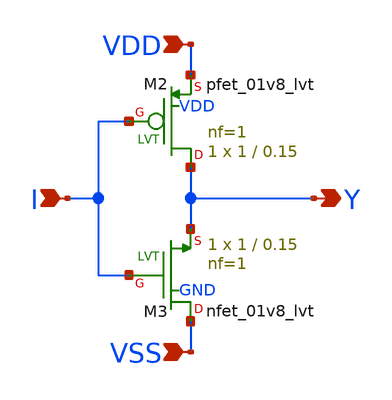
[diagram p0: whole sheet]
** sch_path: xschem/untitled.sch
**.subckt untitled I VDD VSS Y
*.ipin I
*.ipin VDD
*.ipin VSS
*.opin Y
XM2 Y I VDD VDD sky130_fd_pr__pfet_01v8_lvt L=0.15 W=1 nf=1 ad='int((nf+1)/2) * W/nf * 0.29' as='int((nf+2)/2) * W/nf * 0.29'
+ pd='2*int((nf+1)/2) * (W/nf + 0.29)' ps='2*int((nf+2)/2) * (W/nf + 0.29)' nrd='0.29 / W' nrs='0.29 / W'
+ sa=0 sb=0 sd=0 mult=1 m=1
XM3 VSS I Y GND sky130_fd_pr__nfet_01v8_lvt L=0.15 W=1 nf=1 ad='int((nf+1)/2) * W/nf * 0.29' as='int((nf+2)/2) * W/nf * 0.29'
+ pd='2*int((nf+1)/2) * (W/nf + 0.29)' ps='2*int((nf+2)/2) * (W/nf + 0.29)' nrd='0.29 / W' nrs='0.29 / W'
+ sa=0 sb=0 sd=0 mult=1 m=1
**.ends
.end
